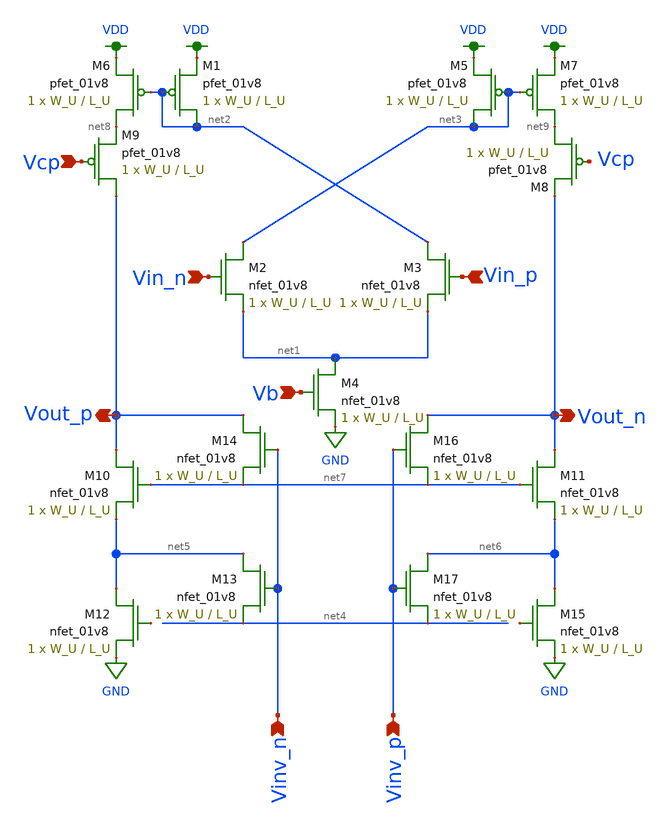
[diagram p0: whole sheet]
** sch_path: schematics/OTA.sch
**.subckt OTA Vcp Vb Vinv_n Vinv_p Vin_n Vin_p Vout_n Vout_p
*.ipin Vcp
*.ipin Vb
*.ipin Vinv_n
*.ipin Vinv_p
*.ipin Vin_n
*.ipin Vin_p
*.opin Vout_n
*.opin Vout_p
XM1 net2 net2 VDD VDD sky130_fd_pr__pfet_01v8 L=L_U W=W_U nf=1 ad='int((nf+1)/2) * W/nf * 0.29' as='int((nf+2)/2) * W/nf * 0.29'
+ pd='2*int((nf+1)/2) * (W/nf + 0.29)' ps='2*int((nf+2)/2) * (W/nf + 0.29)' nrd='0.29 / W' nrs='0.29 / W'
+ sa=0 sb=0 sd=0 mult=1 m=1
XM2 net3 Vin_n net1 GND sky130_fd_pr__nfet_01v8 L=L_U W=W_U nf=1 ad='int((nf+1)/2) * W/nf * 0.29' as='int((nf+2)/2) * W/nf * 0.29'
+ pd='2*int((nf+1)/2) * (W/nf + 0.29)' ps='2*int((nf+2)/2) * (W/nf + 0.29)' nrd='0.29 / W' nrs='0.29 / W'
+ sa=0 sb=0 sd=0 mult=1 m=1
XM3 net2 Vin_p net1 GND sky130_fd_pr__nfet_01v8 L=L_U W=W_U nf=1 ad='int((nf+1)/2) * W/nf * 0.29' as='int((nf+2)/2) * W/nf * 0.29'
+ pd='2*int((nf+1)/2) * (W/nf + 0.29)' ps='2*int((nf+2)/2) * (W/nf + 0.29)' nrd='0.29 / W' nrs='0.29 / W'
+ sa=0 sb=0 sd=0 mult=1 m=1
XM4 net1 Vb GND GND sky130_fd_pr__nfet_01v8 L=L_U W=W_U nf=1 ad='int((nf+1)/2) * W/nf * 0.29' as='int((nf+2)/2) * W/nf * 0.29'
+ pd='2*int((nf+1)/2) * (W/nf + 0.29)' ps='2*int((nf+2)/2) * (W/nf + 0.29)' nrd='0.29 / W' nrs='0.29 / W'
+ sa=0 sb=0 sd=0 mult=1 m=1
XM5 net3 net3 VDD VDD sky130_fd_pr__pfet_01v8 L=L_U W=W_U nf=1 ad='int((nf+1)/2) * W/nf * 0.29' as='int((nf+2)/2) * W/nf * 0.29'
+ pd='2*int((nf+1)/2) * (W/nf + 0.29)' ps='2*int((nf+2)/2) * (W/nf + 0.29)' nrd='0.29 / W' nrs='0.29 / W'
+ sa=0 sb=0 sd=0 mult=1 m=1
XM6 net8 net2 VDD VDD sky130_fd_pr__pfet_01v8 L=L_U W=W_U nf=1 ad='int((nf+1)/2) * W/nf * 0.29' as='int((nf+2)/2) * W/nf * 0.29'
+ pd='2*int((nf+1)/2) * (W/nf + 0.29)' ps='2*int((nf+2)/2) * (W/nf + 0.29)' nrd='0.29 / W' nrs='0.29 / W'
+ sa=0 sb=0 sd=0 mult=1 m=1
XM7 net9 net3 VDD VDD sky130_fd_pr__pfet_01v8 L=L_U W=W_U nf=1 ad='int((nf+1)/2) * W/nf * 0.29' as='int((nf+2)/2) * W/nf * 0.29'
+ pd='2*int((nf+1)/2) * (W/nf + 0.29)' ps='2*int((nf+2)/2) * (W/nf + 0.29)' nrd='0.29 / W' nrs='0.29 / W'
+ sa=0 sb=0 sd=0 mult=1 m=1
XM8 net9 Vcp Vout_n VDD sky130_fd_pr__pfet_01v8 L=L_U W=W_U nf=1 ad='int((nf+1)/2) * W/nf * 0.29' as='int((nf+2)/2) * W/nf * 0.29'
+ pd='2*int((nf+1)/2) * (W/nf + 0.29)' ps='2*int((nf+2)/2) * (W/nf + 0.29)' nrd='0.29 / W' nrs='0.29 / W'
+ sa=0 sb=0 sd=0 mult=1 m=1
XM9 Vout_p Vcp net8 VDD sky130_fd_pr__pfet_01v8 L=L_U W=W_U nf=1 ad='int((nf+1)/2) * W/nf * 0.29' as='int((nf+2)/2) * W/nf * 0.29'
+ pd='2*int((nf+1)/2) * (W/nf + 0.29)' ps='2*int((nf+2)/2) * (W/nf + 0.29)' nrd='0.29 / W' nrs='0.29 / W'
+ sa=0 sb=0 sd=0 mult=1 m=1
XM10 Vout_p net7 net5 GND sky130_fd_pr__nfet_01v8 L=L_U W=W_U nf=1 ad='int((nf+1)/2) * W/nf * 0.29' as='int((nf+2)/2) * W/nf * 0.29'
+ pd='2*int((nf+1)/2) * (W/nf + 0.29)' ps='2*int((nf+2)/2) * (W/nf + 0.29)' nrd='0.29 / W' nrs='0.29 / W'
+ sa=0 sb=0 sd=0 mult=1 m=1
XM11 Vout_n net7 net6 GND sky130_fd_pr__nfet_01v8 L=L_U W=W_U nf=1 ad='int((nf+1)/2) * W/nf * 0.29' as='int((nf+2)/2) * W/nf * 0.29'
+ pd='2*int((nf+1)/2) * (W/nf + 0.29)' ps='2*int((nf+2)/2) * (W/nf + 0.29)' nrd='0.29 / W' nrs='0.29 / W'
+ sa=0 sb=0 sd=0 mult=1 m=1
XM12 net5 net10 GND GND sky130_fd_pr__nfet_01v8 L=L_U W=W_U nf=1 ad='int((nf+1)/2) * W/nf * 0.29' as='int((nf+2)/2) * W/nf * 0.29'
+ pd='2*int((nf+1)/2) * (W/nf + 0.29)' ps='2*int((nf+2)/2) * (W/nf + 0.29)' nrd='0.29 / W' nrs='0.29 / W'
+ sa=0 sb=0 sd=0 mult=1 m=1
XM13 net5 Vinv_n net4 GND sky130_fd_pr__nfet_01v8 L=L_U W=W_U nf=1 ad='int((nf+1)/2) * W/nf * 0.29' as='int((nf+2)/2) * W/nf * 0.29'
+ pd='2*int((nf+1)/2) * (W/nf + 0.29)' ps='2*int((nf+2)/2) * (W/nf + 0.29)' nrd='0.29 / W' nrs='0.29 / W'
+ sa=0 sb=0 sd=0 mult=1 m=1
XM14 Vout_p Vinv_n net7 GND sky130_fd_pr__nfet_01v8 L=L_U W=W_U nf=1 ad='int((nf+1)/2) * W/nf * 0.29'
+ as='int((nf+2)/2) * W/nf * 0.29' pd='2*int((nf+1)/2) * (W/nf + 0.29)' ps='2*int((nf+2)/2) * (W/nf + 0.29)'
+ nrd='0.29 / W' nrs='0.29 / W' sa=0 sb=0 sd=0 mult=1 m=1
XM15 net6 net11 GND GND sky130_fd_pr__nfet_01v8 L=L_U W=W_U nf=1 ad='int((nf+1)/2) * W/nf * 0.29' as='int((nf+2)/2) * W/nf * 0.29'
+ pd='2*int((nf+1)/2) * (W/nf + 0.29)' ps='2*int((nf+2)/2) * (W/nf + 0.29)' nrd='0.29 / W' nrs='0.29 / W'
+ sa=0 sb=0 sd=0 mult=1 m=1
XM16 Vout_n Vinv_p net7 GND sky130_fd_pr__nfet_01v8 L=L_U W=W_U nf=1 ad='int((nf+1)/2) * W/nf * 0.29'
+ as='int((nf+2)/2) * W/nf * 0.29' pd='2*int((nf+1)/2) * (W/nf + 0.29)' ps='2*int((nf+2)/2) * (W/nf + 0.29)'
+ nrd='0.29 / W' nrs='0.29 / W' sa=0 sb=0 sd=0 mult=1 m=1
XM17 net6 Vinv_p net4 GND sky130_fd_pr__nfet_01v8 L=L_U W=W_U nf=1 ad='int((nf+1)/2) * W/nf * 0.29' as='int((nf+2)/2) * W/nf * 0.29'
+ pd='2*int((nf+1)/2) * (W/nf + 0.29)' ps='2*int((nf+2)/2) * (W/nf + 0.29)' nrd='0.29 / W' nrs='0.29 / W'
+ sa=0 sb=0 sd=0 mult=1 m=1
**.ends
.GLOBAL VDD
.GLOBAL GND
.end
